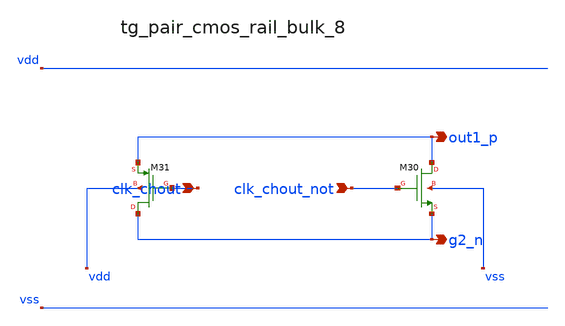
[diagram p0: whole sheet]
** sch_path: analog-db/raw/ia_002_fan_chopper_simple/hier/blocks/tg_pair_cmos_rail_bulk_8.sch
**.subckt tg_pair_cmos_rail_bulk_8 clk_chout clk_chout_not out1_p g2_n
*.ipin clk_chout
*.ipin clk_chout_not
*.opin out1_p
*.opin g2_n
XM30 out1_p clk_chout_not g2_n vss sg13_lv_nmos w=x_dut_xm30_w l=x_dut_xm30_l ng=1 m=x_dut_xm30_m
XM31 g2_n clk_chout out1_p vdd sg13_lv_pmos w=x_dut_xm31_w l=x_dut_xm31_l ng=1 m=x_dut_xm31_m
**.ends
.end
